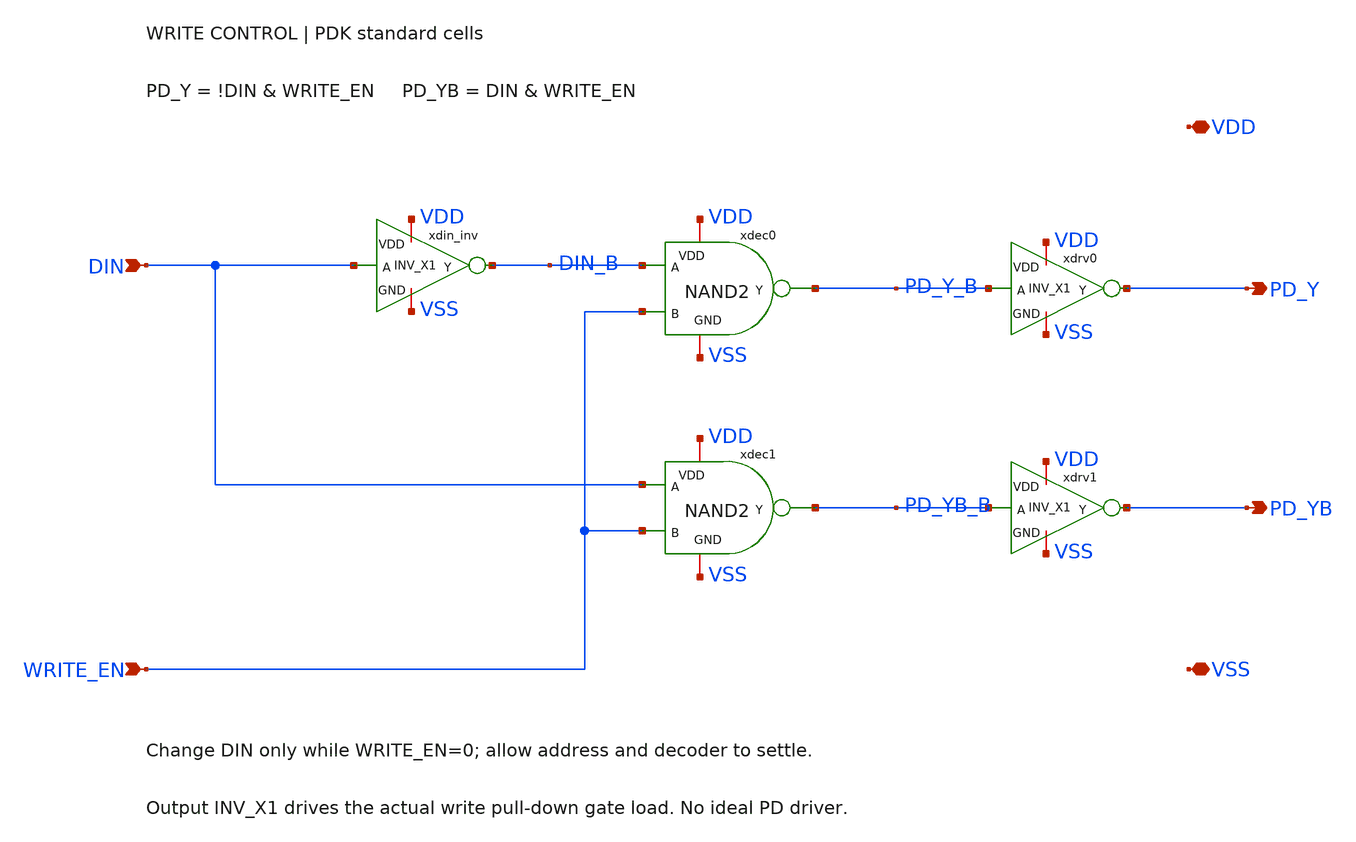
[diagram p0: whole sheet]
** sch_path: member_project/SRAM/PenguinEino/sram512/schematics/write_control.sch
**.subckt write_control DIN WRITE_EN PD_Y PD_YB VDD VSS
*.ipin DIN
*.ipin WRITE_EN
*.opin PD_Y
*.opin PD_YB
*.iopin VDD
*.iopin VSS
xdin_inv VDD DIN DIN_B VSS INV_X1
xdec0 VDD PD_Y_B DIN_B WRITE_EN VSS NAND2
xdrv0 VDD PD_Y_B PD_Y VSS INV_X1
xdec1 VDD PD_YB_B DIN WRITE_EN VSS NAND2
xdrv1 VDD PD_YB_B PD_YB VSS INV_X1
**.ends
.end
